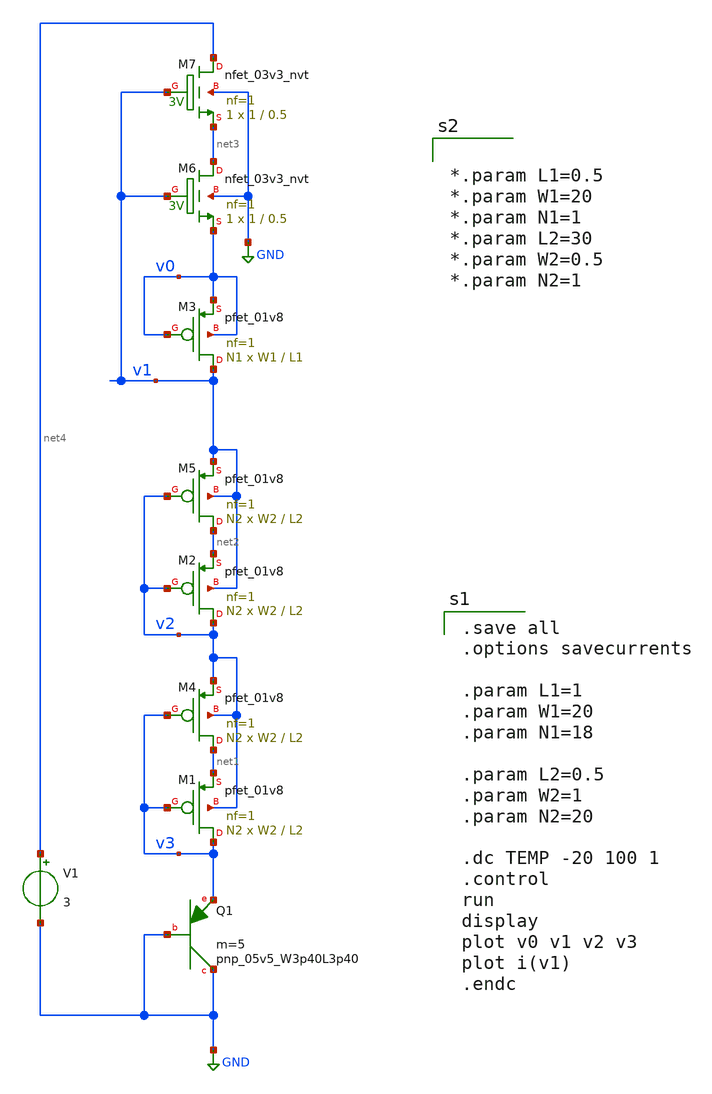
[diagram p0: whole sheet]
** sch_path: SKY130/xschem/cmos_vref/Y.Ji_JSSC2019/s2_ztat1.sch
**.subckt s2_ztat1
XQ1 GND GND v3 sky130_fd_pr__pnp_05v5_W3p40L3p40 m=5
V1 net4 GND 3
XM3 v1 v0 v0 v0 sky130_fd_pr__pfet_01v8 L=L1 W=W1 nf=1 ad='int((nf+1)/2) * W/nf * 0.29' as='int((nf+2)/2) * W/nf * 0.29'
+ pd='2*int((nf+1)/2) * (W/nf + 0.29)' ps='2*int((nf+2)/2) * (W/nf + 0.29)' nrd='0.29 / W' nrs='0.29 / W'
+ sa=0 sb=0 sd=0 mult=N1 m=N1
XM1 v3 v3 net1 v2 sky130_fd_pr__pfet_01v8 L=L2 W=W2 nf=1 ad='int((nf+1)/2) * W/nf * 0.29' as='int((nf+2)/2) * W/nf * 0.29'
+ pd='2*int((nf+1)/2) * (W/nf + 0.29)' ps='2*int((nf+2)/2) * (W/nf + 0.29)' nrd='0.29 / W' nrs='0.29 / W'
+ sa=0 sb=0 sd=0 mult=N2 m=N2
XM4 net1 v3 v2 v2 sky130_fd_pr__pfet_01v8 L=L2 W=W2 nf=1 ad='int((nf+1)/2) * W/nf * 0.29' as='int((nf+2)/2) * W/nf * 0.29'
+ pd='2*int((nf+1)/2) * (W/nf + 0.29)' ps='2*int((nf+2)/2) * (W/nf + 0.29)' nrd='0.29 / W' nrs='0.29 / W'
+ sa=0 sb=0 sd=0 mult=N2 m=N2
XM2 v2 v2 net2 v1 sky130_fd_pr__pfet_01v8 L=L2 W=W2 nf=1 ad='int((nf+1)/2) * W/nf * 0.29' as='int((nf+2)/2) * W/nf * 0.29'
+ pd='2*int((nf+1)/2) * (W/nf + 0.29)' ps='2*int((nf+2)/2) * (W/nf + 0.29)' nrd='0.29 / W' nrs='0.29 / W'
+ sa=0 sb=0 sd=0 mult=N2 m=N2
XM5 net2 v2 v1 v1 sky130_fd_pr__pfet_01v8 L=L2 W=W2 nf=1 ad='int((nf+1)/2) * W/nf * 0.29' as='int((nf+2)/2) * W/nf * 0.29'
+ pd='2*int((nf+1)/2) * (W/nf + 0.29)' ps='2*int((nf+2)/2) * (W/nf + 0.29)' nrd='0.29 / W' nrs='0.29 / W'
+ sa=0 sb=0 sd=0 mult=N2 m=N2
XM6 net3 v1 v0 GND sky130_fd_pr__nfet_03v3_nvt L=0.5 W=1 nf=1 ad='int((nf+1)/2) * W/nf * 0.29' as='int((nf+2)/2) * W/nf * 0.29'
+ pd='2*int((nf+1)/2) * (W/nf + 0.29)' ps='2*int((nf+2)/2) * (W/nf + 0.29)' nrd='0.29 / W' nrs='0.29 / W'
+ sa=0 sb=0 sd=0 mult=1 m=1
XM7 net4 v1 net3 GND sky130_fd_pr__nfet_03v3_nvt L=0.5 W=1 nf=1 ad='int((nf+1)/2) * W/nf * 0.29' as='int((nf+2)/2) * W/nf * 0.29'
+ pd='2*int((nf+1)/2) * (W/nf + 0.29)' ps='2*int((nf+2)/2) * (W/nf + 0.29)' nrd='0.29 / W' nrs='0.29 / W'
+ sa=0 sb=0 sd=0 mult=1 m=1
**** begin user architecture code
.lib $::SKYWATER_MODELS/sky130.lib.spice tt
.include $::PDKPATH/libs.ref/sky130_fd_sc_hvl/spice/sky130_fd_sc_hvl.spice

.save all
.options savecurrents

.param L1=1
.param W1=20
.param N1=18

.param L2=0.5
.param W2=1
.param N2=20

.dc TEMP -20 100 1
.control
run
display
plot v0 v1 v2 v3
plot i(v1)
.endc




*.param L1=0.5
*.param W1=20
*.param N1=1
*.param L2=30
*.param W2=0.5
*.param N2=1



**** end user architecture code
**.ends
.GLOBAL GND
.end
